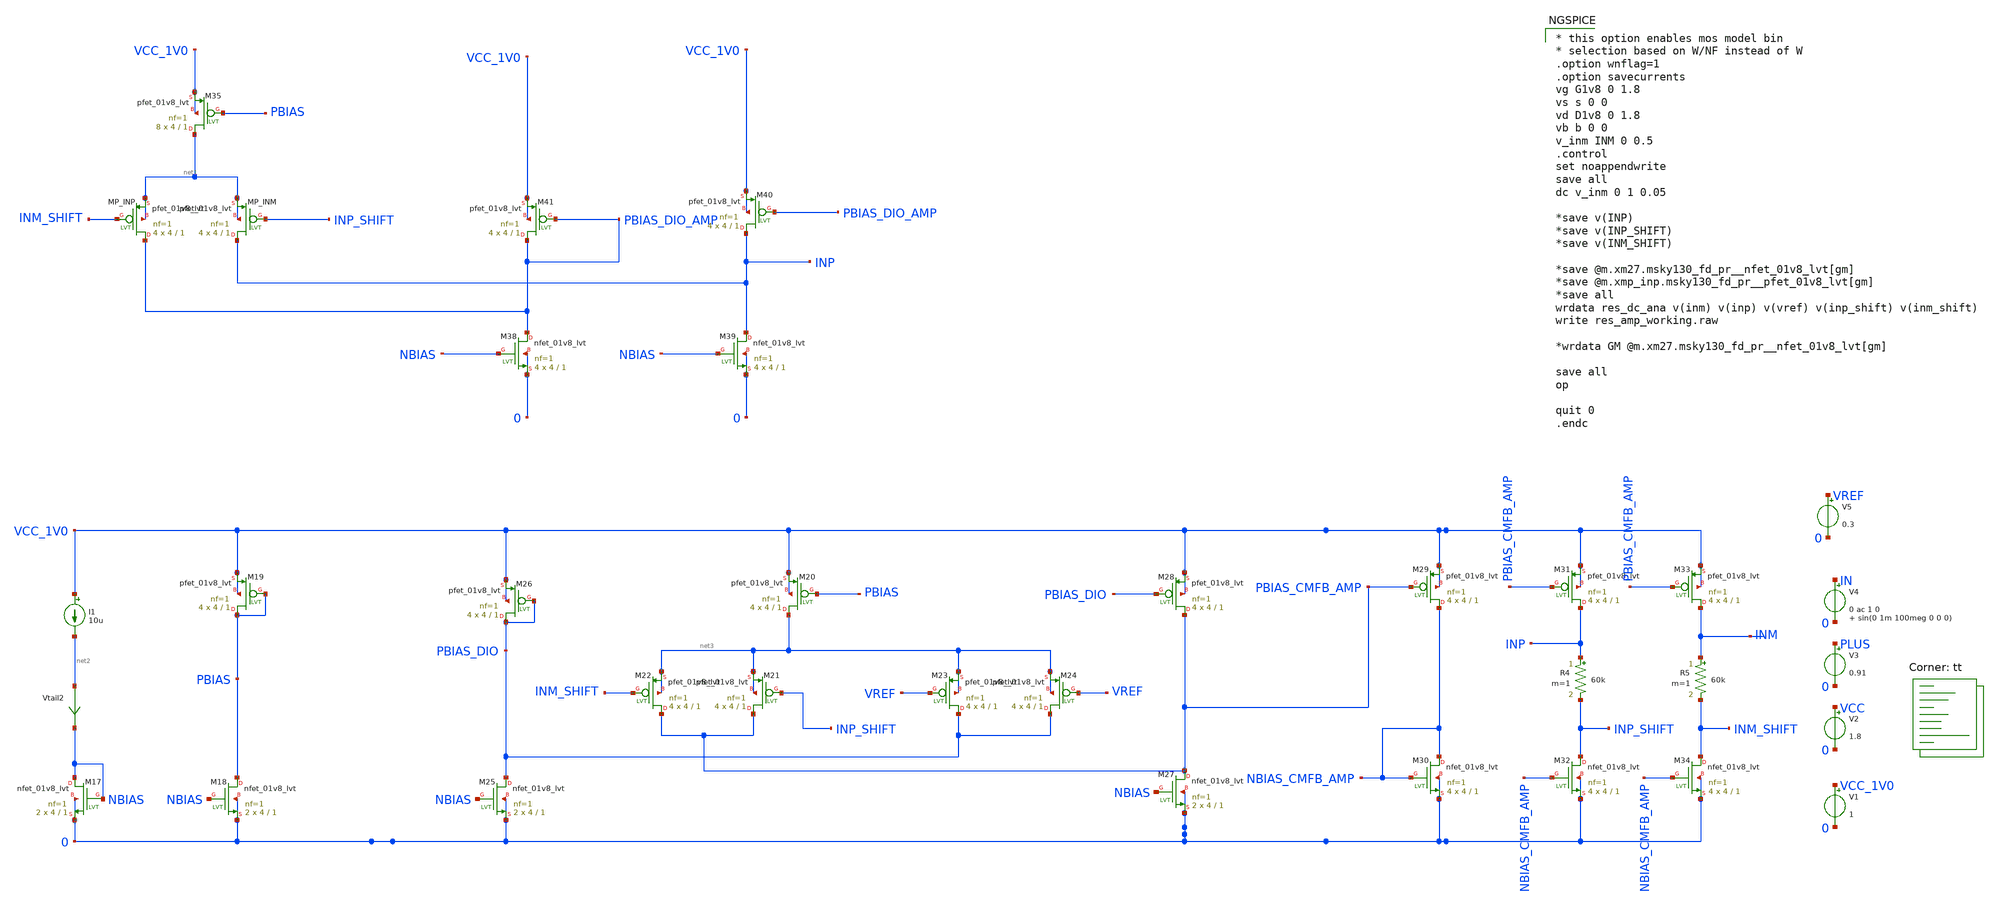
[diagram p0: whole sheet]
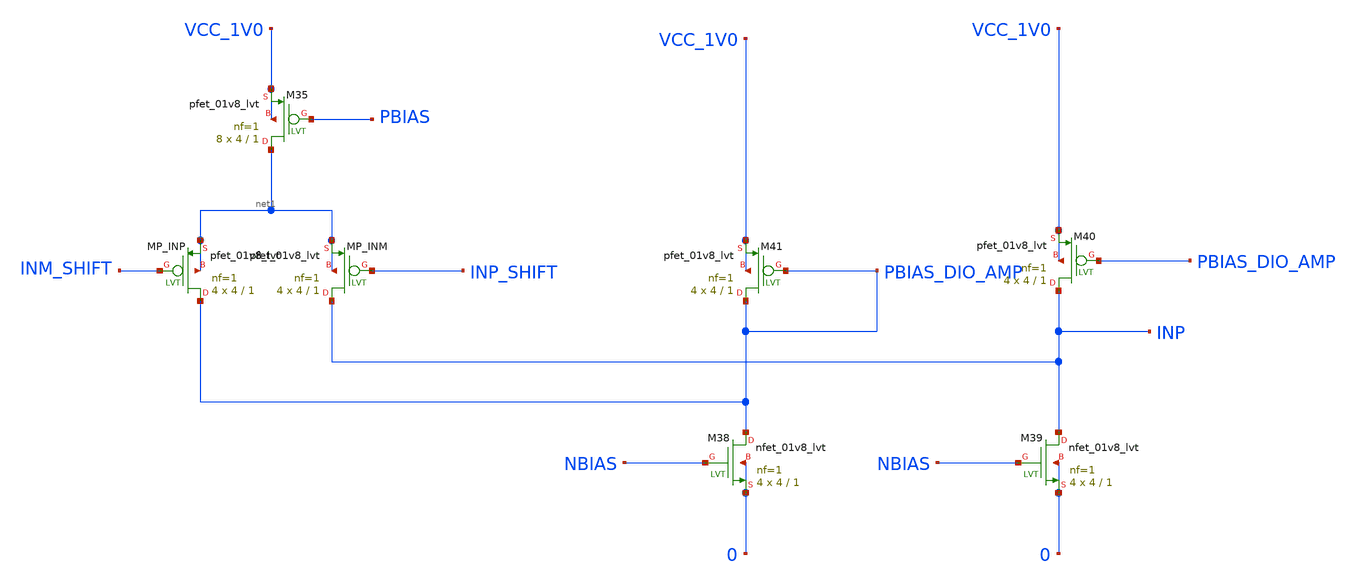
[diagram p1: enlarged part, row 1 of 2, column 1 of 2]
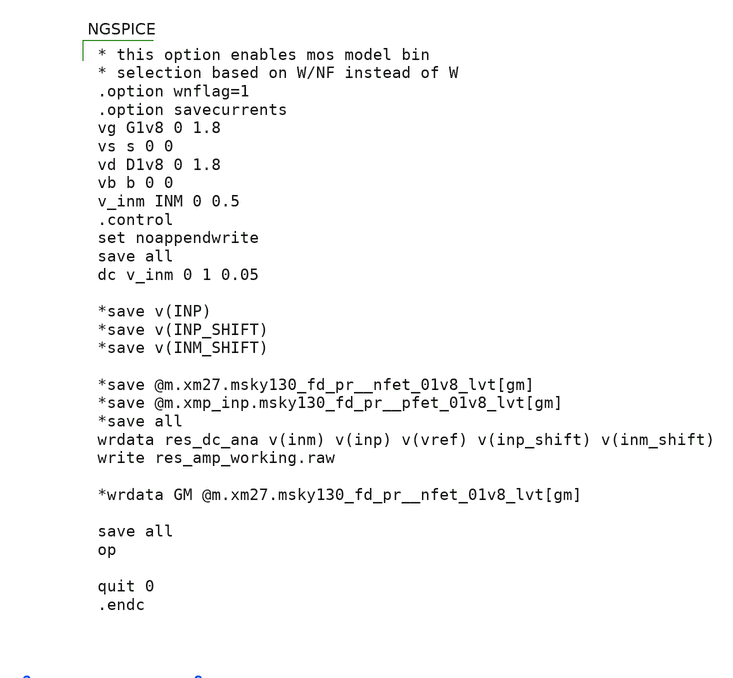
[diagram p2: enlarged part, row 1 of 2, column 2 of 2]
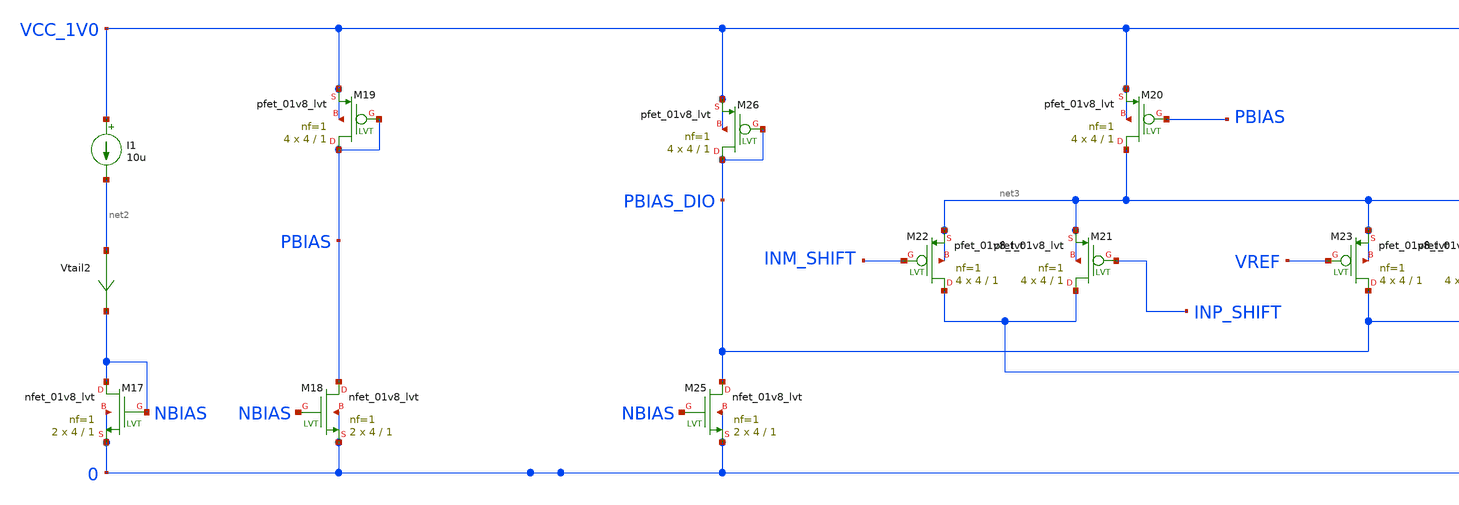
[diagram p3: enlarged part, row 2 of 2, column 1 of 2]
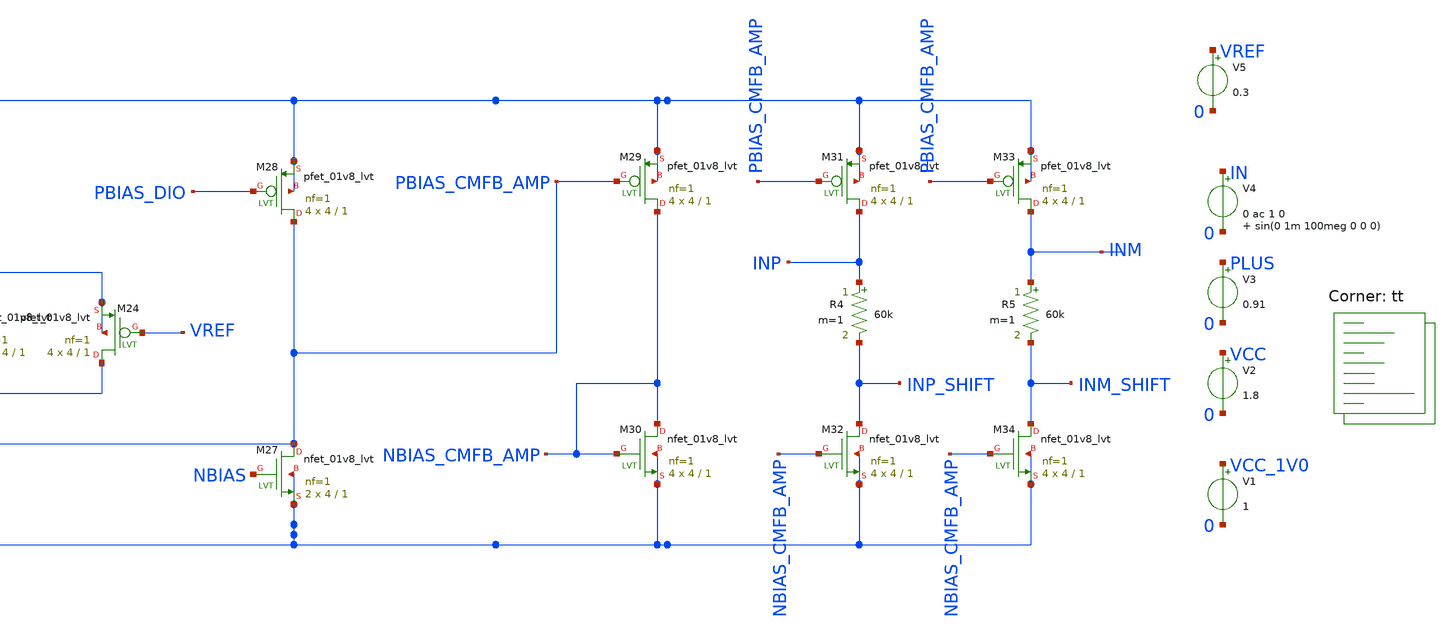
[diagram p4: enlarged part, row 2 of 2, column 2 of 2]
** sch_path: Res_amp/res_amp_working.sch
* Copyright 2021 Stefan Frederik Schippers
* Licensed under the Apache License, Version 2.0 (the "License");
* you may not use this file except in compliance with the License.
* You may obtain a copy of the License at
* https://www.apache.org/licenses/LICENSE-2.0
* Unless required by applicable law or agreed to in writing, software
* distributed under the License is distributed on an "AS IS" BASIS,
* WITHOUT WARRANTIES OR CONDITIONS OF ANY KIND, either express or implied.
* See the License for the specific language governing permissions and
* limitations under the License.
**.subckt res_amp_working
V2 VCC 0 1.8
V3 PLUS 0 0.91
V4 IN 0 0 ac 1 0 sin(0 1m 100meg 0 0 0)
V1 VCC_1V0 0 1
V5 VREF 0 0.3
XM35 net1 PBIAS VCC_1V0 VCC_1V0 sky130_fd_pr__pfet_01v8_lvt L=1 W=4 nf=1 ad='int((1 + 1)/2) * 4 / 1 * 0.29'
+ as='int((1 + 2)/2) * 4 / 1 * 0.29' pd='2*int((1 + 1)/2) * (4 / 1 + 0.29)' ps='2*int((1 + 2)/2) * (4 / 1 + 0.29)'
+ nrd='0.29 / 4 ' nrs='0.29 / 4 ' sa=0 sb=0 sd=0 mult=8 m=8
XMP_INM INP INP_SHIFT net1 net1 sky130_fd_pr__pfet_01v8_lvt L=1 W=4 nf=1 ad='int((1 + 1)/2) * 4 / 1 * 0.29'
+ as='int((1 + 2)/2) * 4 / 1 * 0.29' pd='2*int((1 + 1)/2) * (4 / 1 + 0.29)' ps='2*int((1 + 2)/2) * (4 / 1 + 0.29)'
+ nrd='0.29 / 4 ' nrs='0.29 / 4 ' sa=0 sb=0 sd=0 mult=4 m=4
XMP_INP PBIAS_DIO_AMP INM_SHIFT net1 net1 sky130_fd_pr__pfet_01v8_lvt L=1 W=4 nf=1 ad='int((1 + 1)/2) * 4 / 1 * 0.29'
+ as='int((1 + 2)/2) * 4 / 1 * 0.29' pd='2*int((1 + 1)/2) * (4 / 1 + 0.29)' ps='2*int((1 + 2)/2) * (4 / 1 + 0.29)'
+ nrd='0.29 / 4 ' nrs='0.29 / 4 ' sa=0 sb=0 sd=0 mult=4 m=4
XM38 PBIAS_DIO_AMP NBIAS 0 0 sky130_fd_pr__nfet_01v8_lvt L=1 W=4 nf=1 ad='int((1 + 1)/2) * 4 / 1 * 0.29'
+ as='int((1 + 2)/2) * 4 / 1 * 0.29' pd='2*int((1 + 1)/2) * (4 / 1 + 0.29)' ps='2*int((1 + 2)/2) * (4 / 1 + 0.29)'
+ nrd='0.29 / 4 ' nrs='0.29 / 4 ' sa=0 sb=0 sd=0 mult=4 m=4
XM39 INP NBIAS 0 0 sky130_fd_pr__nfet_01v8_lvt L=1 W=4 nf=1 ad='int((1 + 1)/2) * 4 / 1 * 0.29' as='int((1 + 2)/2) * 4 / 1 * 0.29'
+ pd='2*int((1 + 1)/2) * (4 / 1 + 0.29)' ps='2*int((1 + 2)/2) * (4 / 1 + 0.29)' nrd='0.29 / 4 ' nrs='0.29 / 4 '
+ sa=0 sb=0 sd=0 mult=4 m=4
XM40 INP PBIAS_DIO_AMP VCC_1V0 VCC_1V0 sky130_fd_pr__pfet_01v8_lvt L=1 W=4 nf=1 ad='int((1 + 1)/2) * 4 / 1 * 0.29'
+ as='int((1 + 2)/2) * 4 / 1 * 0.29' pd='2*int((1 + 1)/2) * (4 / 1 + 0.29)' ps='2*int((1 + 2)/2) * (4 / 1 + 0.29)'
+ nrd='0.29 / 4 ' nrs='0.29 / 4 ' sa=0 sb=0 sd=0 mult=4 m=4
XM41 PBIAS_DIO_AMP PBIAS_DIO_AMP VCC_1V0 VCC_1V0 sky130_fd_pr__pfet_01v8_lvt L=1 W=4 nf=1 ad='int((1 + 1)/2) * 4 / 1 * 0.29'
+ as='int((1 + 2)/2) * 4 / 1 * 0.29' pd='2*int((1 + 1)/2) * (4 / 1 + 0.29)' ps='2*int((1 + 2)/2) * (4 / 1 + 0.29)'
+ nrd='0.29 / 4 ' nrs='0.29 / 4 ' sa=0 sb=0 sd=0 mult=4 m=4
XM17 NBIAS NBIAS 0 0 sky130_fd_pr__nfet_01v8_lvt L=1 W=4 nf=1 ad='int((1 + 1)/2) * 4 / 1 * 0.29' as='int((1 + 2)/2) * 4 / 1 * 0.29'
+ pd='2*int((1 + 1)/2) * (4 / 1 + 0.29)' ps='2*int((1 + 2)/2) * (4 / 1 + 0.29)' nrd='0.29 / 4 ' nrs='0.29 / 4 '
+ sa=0 sb=0 sd=0 mult=2 m=2
Vtail2 net2 NBIAS 0
.save i(vtail2)
I1 VCC_1V0 net2 10u
XM18 PBIAS NBIAS 0 0 sky130_fd_pr__nfet_01v8_lvt L=1 W=4 nf=1 ad='int((1 + 1)/2) * 4 / 1 * 0.29' as='int((1 + 2)/2) * 4 / 1 * 0.29'
+ pd='2*int((1 + 1)/2) * (4 / 1 + 0.29)' ps='2*int((1 + 2)/2) * (4 / 1 + 0.29)' nrd='0.29 / 4 ' nrs='0.29 / 4 '
+ sa=0 sb=0 sd=0 mult=2 m=2
XM19 PBIAS PBIAS VCC_1V0 VCC_1V0 sky130_fd_pr__pfet_01v8_lvt L=1 W=4 nf=1 ad='int((1 + 1)/2) * 4 / 1 * 0.29'
+ as='int((1 + 2)/2) * 4 / 1 * 0.29' pd='2*int((1 + 1)/2) * (4 / 1 + 0.29)' ps='2*int((1 + 2)/2) * (4 / 1 + 0.29)'
+ nrd='0.29 / 4 ' nrs='0.29 / 4 ' sa=0 sb=0 sd=0 mult=4 m=4
XM20 net3 PBIAS VCC_1V0 VCC_1V0 sky130_fd_pr__pfet_01v8_lvt L=1 W=4 nf=1 ad='int((1 + 1)/2) * 4 / 1 * 0.29'
+ as='int((1 + 2)/2) * 4 / 1 * 0.29' pd='2*int((1 + 1)/2) * (4 / 1 + 0.29)' ps='2*int((1 + 2)/2) * (4 / 1 + 0.29)'
+ nrd='0.29 / 4 ' nrs='0.29 / 4 ' sa=0 sb=0 sd=0 mult=4 m=4
XM21 PBIAS_CMFB_AMP INP_SHIFT net3 net3 sky130_fd_pr__pfet_01v8_lvt L=1 W=4 nf=1 ad='int((1 + 1)/2) * 4 / 1 * 0.29'
+ as='int((1 + 2)/2) * 4 / 1 * 0.29' pd='2*int((1 + 1)/2) * (4 / 1 + 0.29)' ps='2*int((1 + 2)/2) * (4 / 1 + 0.29)'
+ nrd='0.29 / 4 ' nrs='0.29 / 4 ' sa=0 sb=0 sd=0 mult=4 m=4
XM22 PBIAS_CMFB_AMP INM_SHIFT net3 net3 sky130_fd_pr__pfet_01v8_lvt L=1 W=4 nf=1 ad='int((1 + 1)/2) * 4 / 1 * 0.29'
+ as='int((1 + 2)/2) * 4 / 1 * 0.29' pd='2*int((1 + 1)/2) * (4 / 1 + 0.29)' ps='2*int((1 + 2)/2) * (4 / 1 + 0.29)'
+ nrd='0.29 / 4 ' nrs='0.29 / 4 ' sa=0 sb=0 sd=0 mult=4 m=4
XM23 PBIAS_DIO VREF net3 net3 sky130_fd_pr__pfet_01v8_lvt L=1 W=4 nf=1 ad='int((1 + 1)/2) * 4 / 1 * 0.29'
+ as='int((1 + 2)/2) * 4 / 1 * 0.29' pd='2*int((1 + 1)/2) * (4 / 1 + 0.29)' ps='2*int((1 + 2)/2) * (4 / 1 + 0.29)'
+ nrd='0.29 / 4 ' nrs='0.29 / 4 ' sa=0 sb=0 sd=0 mult=4 m=4
XM24 PBIAS_DIO VREF net3 net3 sky130_fd_pr__pfet_01v8_lvt L=1 W=4 nf=1 ad='int((1 + 1)/2) * 4 / 1 * 0.29'
+ as='int((1 + 2)/2) * 4 / 1 * 0.29' pd='2*int((1 + 1)/2) * (4 / 1 + 0.29)' ps='2*int((1 + 2)/2) * (4 / 1 + 0.29)'
+ nrd='0.29 / 4 ' nrs='0.29 / 4 ' sa=0 sb=0 sd=0 mult=4 m=4
XM25 PBIAS_DIO NBIAS 0 0 sky130_fd_pr__nfet_01v8_lvt L=1 W=4 nf=1 ad='int((1 + 1)/2) * 4 / 1 * 0.29'
+ as='int((1 + 2)/2) * 4 / 1 * 0.29' pd='2*int((1 + 1)/2) * (4 / 1 + 0.29)' ps='2*int((1 + 2)/2) * (4 / 1 + 0.29)'
+ nrd='0.29 / 4 ' nrs='0.29 / 4 ' sa=0 sb=0 sd=0 mult=2 m=2
XM26 PBIAS_DIO PBIAS_DIO VCC_1V0 VCC_1V0 sky130_fd_pr__pfet_01v8_lvt L=1 W=4 nf=1 ad='int((1 + 1)/2) * 4 / 1 * 0.29'
+ as='int((1 + 2)/2) * 4 / 1 * 0.29' pd='2*int((1 + 1)/2) * (4 / 1 + 0.29)' ps='2*int((1 + 2)/2) * (4 / 1 + 0.29)'
+ nrd='0.29 / 4 ' nrs='0.29 / 4 ' sa=0 sb=0 sd=0 mult=4 m=4
XM27 PBIAS_CMFB_AMP NBIAS 0 0 sky130_fd_pr__nfet_01v8_lvt L=1 W=4 nf=1 ad='int((1 + 1)/2) * 4 / 1 * 0.29'
+ as='int((1 + 2)/2) * 4 / 1 * 0.29' pd='2*int((1 + 1)/2) * (4 / 1 + 0.29)' ps='2*int((1 + 2)/2) * (4 / 1 + 0.29)'
+ nrd='0.29 / 4 ' nrs='0.29 / 4 ' sa=0 sb=0 sd=0 mult=2 m=2
XM28 PBIAS_CMFB_AMP PBIAS_DIO VCC_1V0 VCC_1V0 sky130_fd_pr__pfet_01v8_lvt L=1 W=4 nf=1 ad='int((1 + 1)/2) * 4 / 1 * 0.29'
+ as='int((1 + 2)/2) * 4 / 1 * 0.29' pd='2*int((1 + 1)/2) * (4 / 1 + 0.29)' ps='2*int((1 + 2)/2) * (4 / 1 + 0.29)'
+ nrd='0.29 / 4 ' nrs='0.29 / 4 ' sa=0 sb=0 sd=0 mult=4 m=4
XM29 NBIAS_CMFB_AMP PBIAS_CMFB_AMP VCC_1V0 VCC_1V0 sky130_fd_pr__pfet_01v8_lvt L=1 W=4 nf=1 ad='int((1 + 1)/2) * 4 / 1 * 0.29'
+ as='int((1 + 2)/2) * 4 / 1 * 0.29' pd='2*int((1 + 1)/2) * (4 / 1 + 0.29)' ps='2*int((1 + 2)/2) * (4 / 1 + 0.29)'
+ nrd='0.29 / 4 ' nrs='0.29 / 4 ' sa=0 sb=0 sd=0 mult=4 m=4
XM30 NBIAS_CMFB_AMP NBIAS_CMFB_AMP 0 0 sky130_fd_pr__nfet_01v8_lvt L=1 W=4 nf=1 ad='int((1 + 1)/2) * 4 / 1 * 0.29'
+ as='int((1 + 2)/2) * 4 / 1 * 0.29' pd='2*int((1 + 1)/2) * (4 / 1 + 0.29)' ps='2*int((1 + 2)/2) * (4 / 1 + 0.29)'
+ nrd='0.29 / 4 ' nrs='0.29 / 4 ' sa=0 sb=0 sd=0 mult=4 m=4
XM31 INP PBIAS_CMFB_AMP VCC_1V0 VCC_1V0 sky130_fd_pr__pfet_01v8_lvt L=1 W=4 nf=1 ad='int((1 + 1)/2) * 4 / 1 * 0.29'
+ as='int((1 + 2)/2) * 4 / 1 * 0.29' pd='2*int((1 + 1)/2) * (4 / 1 + 0.29)' ps='2*int((1 + 2)/2) * (4 / 1 + 0.29)'
+ nrd='0.29 / 4 ' nrs='0.29 / 4 ' sa=0 sb=0 sd=0 mult=4 m=4
XM32 INP_SHIFT NBIAS_CMFB_AMP 0 0 sky130_fd_pr__nfet_01v8_lvt L=1 W=4 nf=1 ad='int((1 + 1)/2) * 4 / 1 * 0.29'
+ as='int((1 + 2)/2) * 4 / 1 * 0.29' pd='2*int((1 + 1)/2) * (4 / 1 + 0.29)' ps='2*int((1 + 2)/2) * (4 / 1 + 0.29)'
+ nrd='0.29 / 4 ' nrs='0.29 / 4 ' sa=0 sb=0 sd=0 mult=4 m=4
XM33 INM PBIAS_CMFB_AMP VCC_1V0 VCC_1V0 sky130_fd_pr__pfet_01v8_lvt L=1 W=4 nf=1 ad='int((1 + 1)/2) * 4 / 1 * 0.29'
+ as='int((1 + 2)/2) * 4 / 1 * 0.29' pd='2*int((1 + 1)/2) * (4 / 1 + 0.29)' ps='2*int((1 + 2)/2) * (4 / 1 + 0.29)'
+ nrd='0.29 / 4 ' nrs='0.29 / 4 ' sa=0 sb=0 sd=0 mult=4 m=4
XM34 INM_SHIFT NBIAS_CMFB_AMP 0 0 sky130_fd_pr__nfet_01v8_lvt L=1 W=4 nf=1 ad='int((1 + 1)/2) * 4 / 1 * 0.29'
+ as='int((1 + 2)/2) * 4 / 1 * 0.29' pd='2*int((1 + 1)/2) * (4 / 1 + 0.29)' ps='2*int((1 + 2)/2) * (4 / 1 + 0.29)'
+ nrd='0.29 / 4 ' nrs='0.29 / 4 ' sa=0 sb=0 sd=0 mult=4 m=4
R4 INP INP_SHIFT 60k m=1
R5 INM INM_SHIFT 60k m=1
**** begin user architecture code

* this option enables mos model bin
* selection based on W/NF instead of W
.option wnflag=1
.option savecurrents
vg G1v8 0 1.8
vs s 0 0
vd D1v8 0 1.8
vb b 0 0
v_inm INM 0 0.5
.control
set noappendwrite
save all
dc v_inm 0 1 0.05

*save v(INP)
*save v(INP_SHIFT)
*save v(INM_SHIFT)

*save @m.xm27.msky130_fd_pr__nfet_01v8_lvt[gm]
*save @m.xmp_inp.msky130_fd_pr__pfet_01v8_lvt[gm]
*save all
wrdata res_dc_ana v(inm) v(inp) v(vref) v(inp_shift) v(inm_shift)
write res_amp_working.raw

*wrdata GM @m.xm27.msky130_fd_pr__nfet_01v8_lvt[gm]

save all
op

quit 0
.endc


.lib $::SKYWATER_MODELS/sky130.lib.spice tt
**** end user architecture code
**.ends
.end
